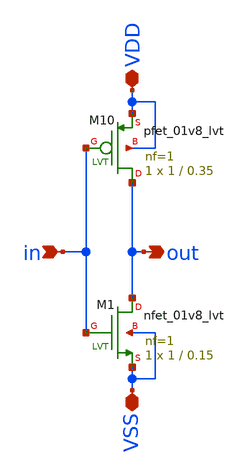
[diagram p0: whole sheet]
** sch_path: xschem/not/not.sch
**.subckt not in out VDD VSS
*.ipin in
*.opin out
*.iopin VDD
*.iopin VSS
XM10 out in VDD VDD sky130_fd_pr__pfet_01v8_lvt L=0.35 W=1 nf=1 ad='int((1 + 1)/2) * 1 / 1 * 0.29' as='int((1 + 2)/2) * 1 / 1 * 0.29'
+ pd='2*int((1 + 1)/2) * (1 / 1 + 0.29)' ps='2*int((1 + 2)/2) * (1 / 1 + 0.29)' nrd='0.29 / 1 ' nrs='0.29 / 1 '
+ sa=0 sb=0 sd=0 mult=1 m=1
XM1 out in VSS VSS sky130_fd_pr__nfet_01v8_lvt L=0.15 W=1 nf=1 ad='int((1 + 1)/2) * 1 / 1 * 0.29' as='int((1 + 2)/2) * 1 / 1 * 0.29'
+ pd='2*int((1 + 1)/2) * (1 / 1 + 0.29)' ps='2*int((1 + 2)/2) * (1 / 1 + 0.29)' nrd='0.29 / 1 ' nrs='0.29 / 1 '
+ sa=0 sb=0 sd=0 mult=1 m=1
**.ends
.end
